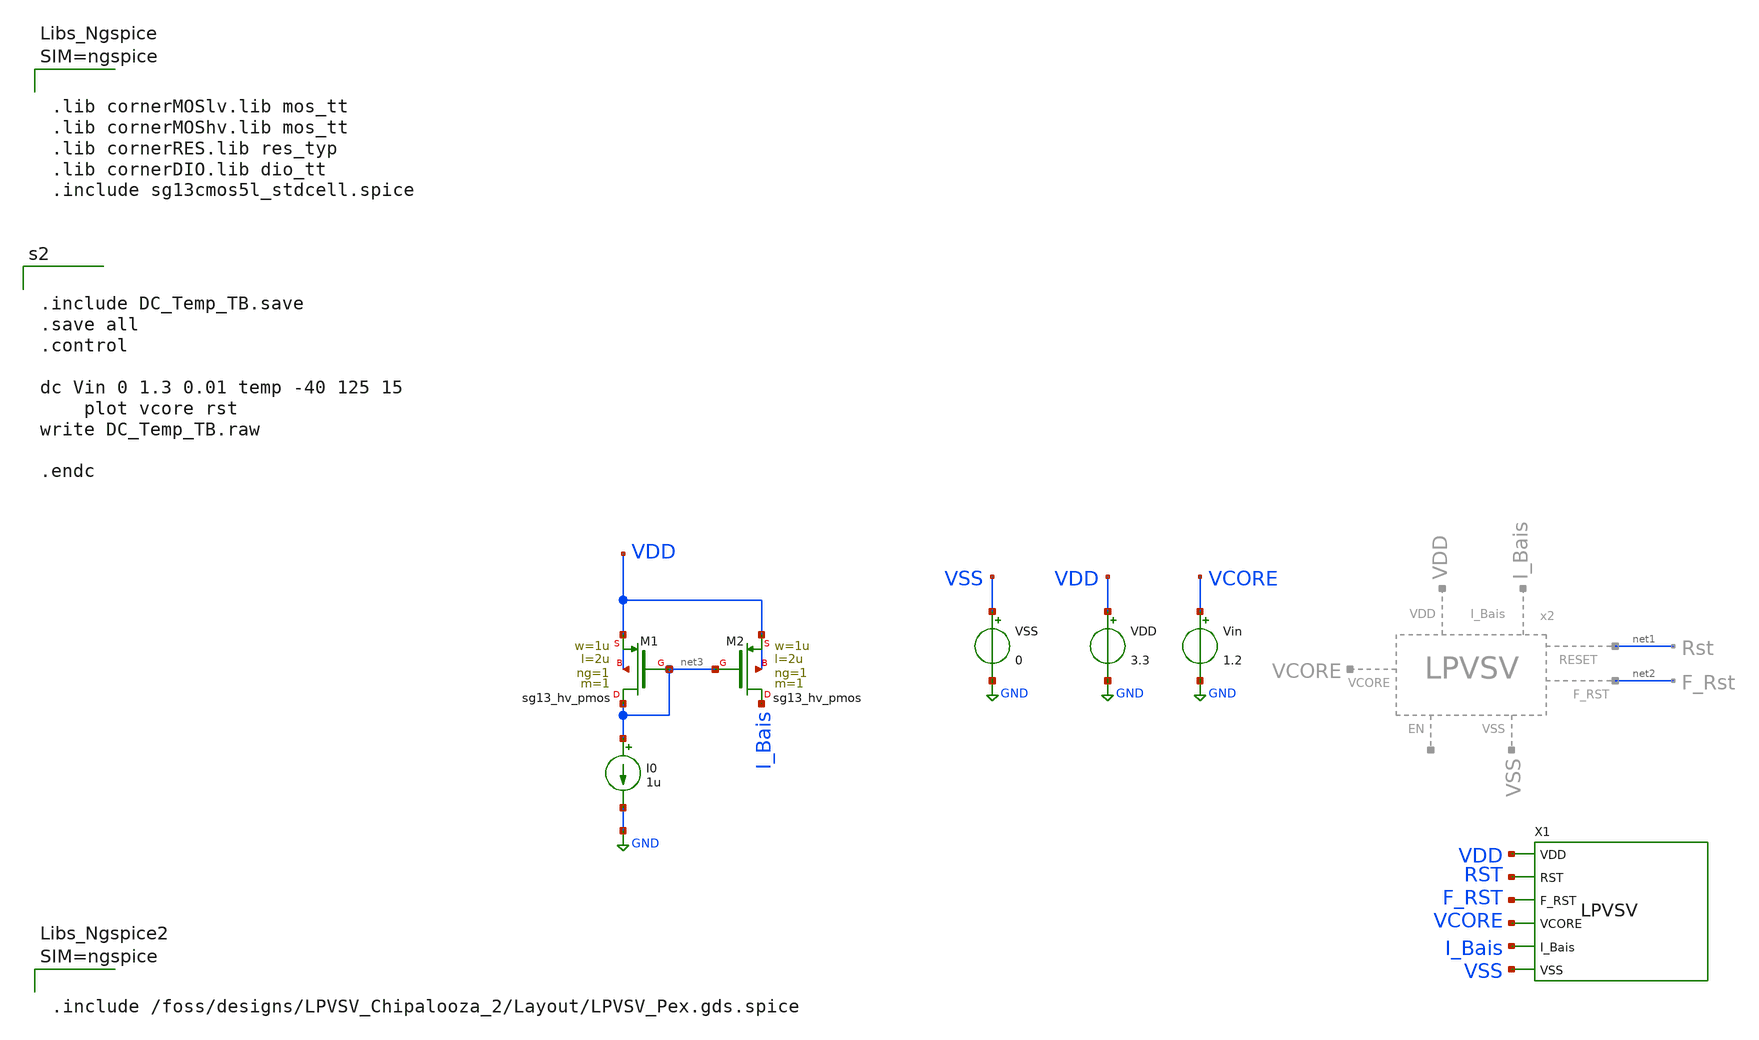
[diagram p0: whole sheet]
** sch_path: Simulation/DC_Temp_TB.sch
**.subckt DC_Temp_TB
VDD VDD GND 3.3
VSS VSS GND 0
Vin VCORE GND 1.2
X1 VSS F_RST VDD VCORE I_Bais RST LPVSV
I0 net3 GND 1u
XM1 net3 net3 VDD VDD sg13_hv_pmos w=1u l=2u ng=1 m=1 mm_ok=1
XM2 I_Bais net3 VDD VDD sg13_hv_pmos w=1u l=2u ng=1 m=1 mm_ok=1
**** begin user architecture code


.include DC_Temp_TB.save
.save all
.control

dc Vin 0 1.3 0.01 temp -40 125 15
	plot vcore rst
write DC_Temp_TB.raw

.endc




.options rshunt = 1e15
.options gmin=1e-9
.options reltol = 0.01 abstol = 1p
.option filetype=ascii





.lib cornerMOSlv.lib mos_tt
.lib cornerMOShv.lib mos_tt
.lib cornerRES.lib res_typ
.lib cornerDIO.lib dio_tt
.include sg13cmos5l_stdcell.spice






.include /foss/designs/LPVSV_Chipalooza_2/Layout/LPVSV_Pex.gds.spice



**** end user architecture code
**.ends
.GLOBAL GND
.end
